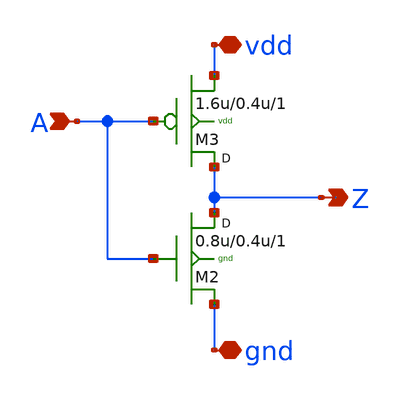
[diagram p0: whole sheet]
** sch_path: sram_2_16_scn4m/pinv_11.sch
**.subckt pinv_11 A Z vdd gnd
*.ipin A
*.opin Z
*.iopin vdd
*.iopin gnd
M2 Z A gnd gnd n w=0.8u l=0.4u m=1
M3 Z A vdd vdd p w=1.6u l=0.4u m=1
**.ends
.end
